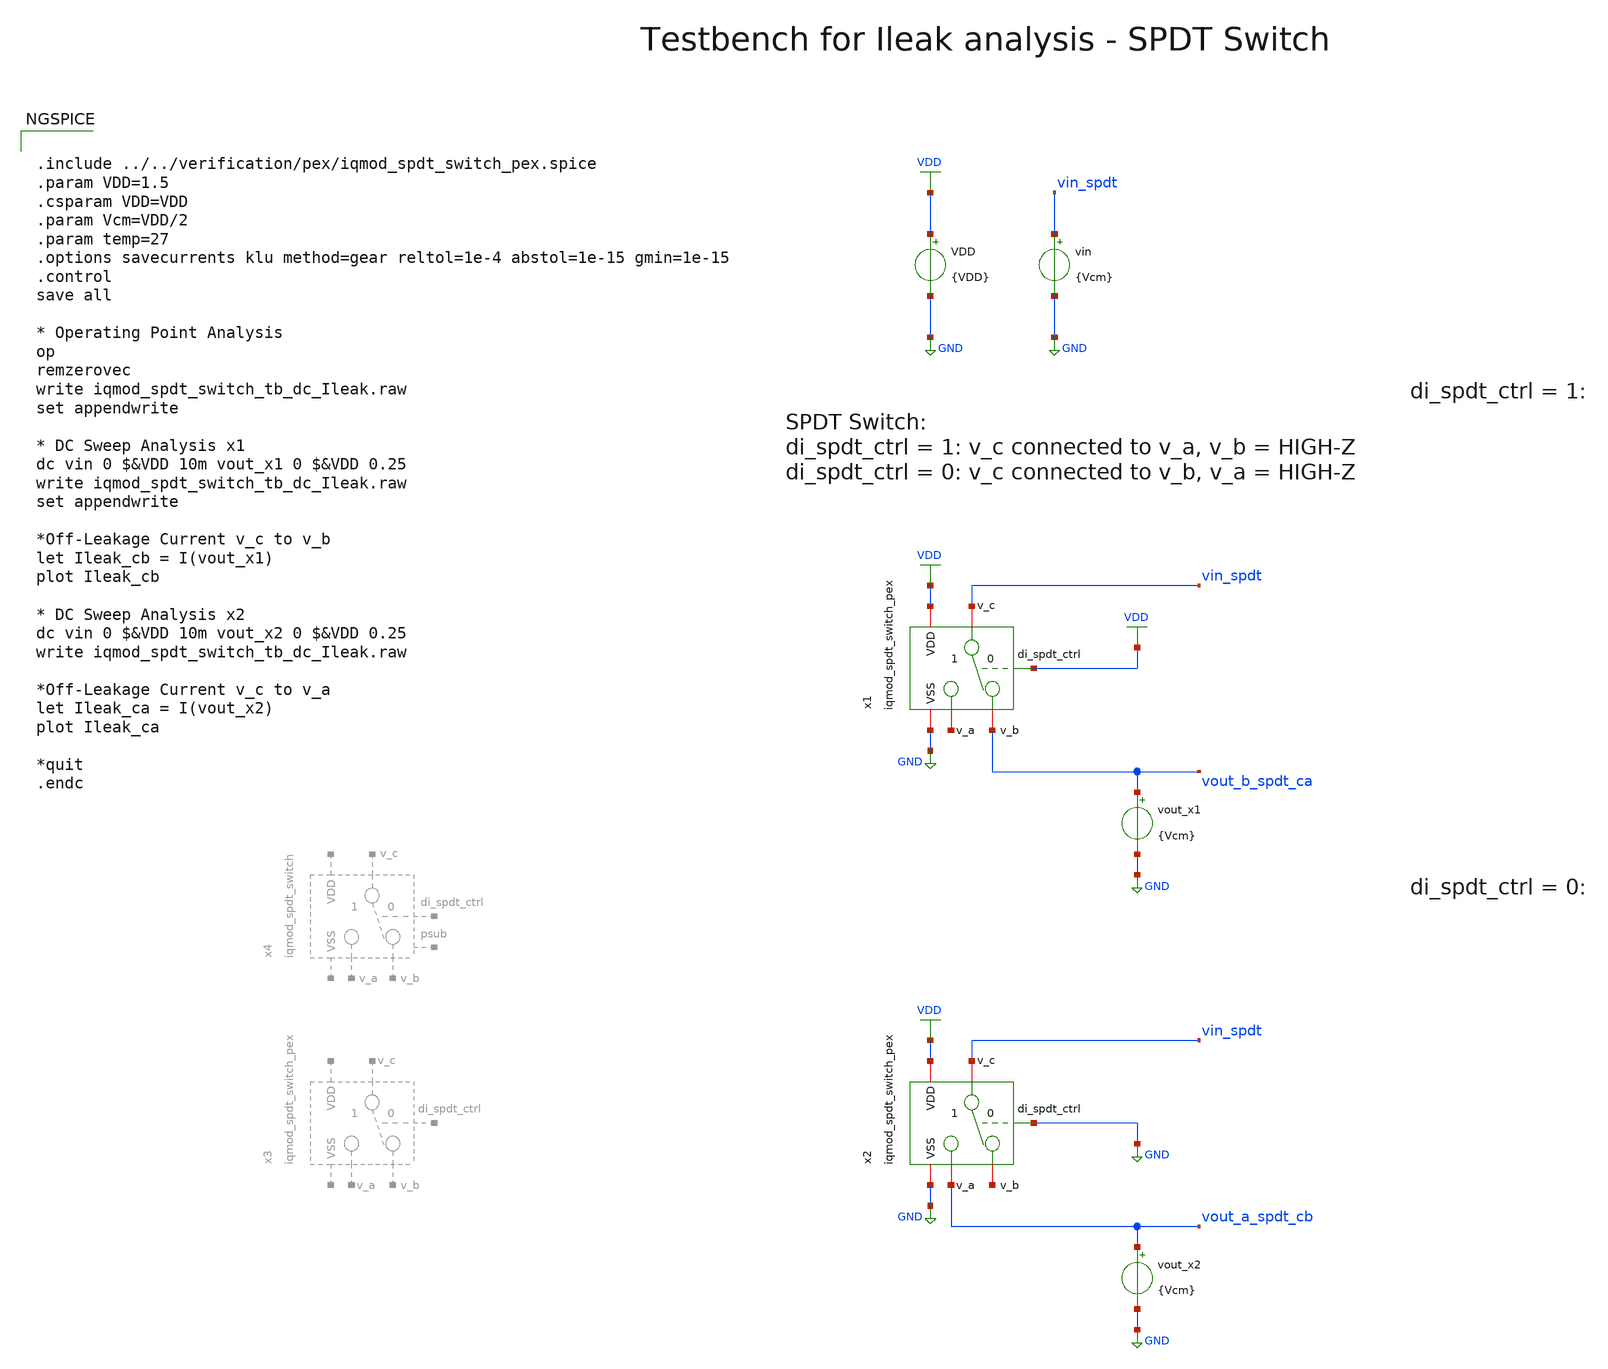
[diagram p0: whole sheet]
** sch_path: ihp130/macros/iqmod/xschem/testbenches/iqmod_spdt_switch_tb_dc_Ileak.sch
**.subckt iqmod_spdt_switch_tb_dc_Ileak
vout_x1 vout_b_spdt_ca GND {Vcm}
vout_x2 vout_a_spdt_cb GND {Vcm}
vin vin_spdt GND {Vcm}
VDD VDD GND {VDD}
x1 VDD VDD GND vin_spdt vout_b_spdt_ca net1 iqmod_spdt_switch_pex
x2 VDD GND GND vin_spdt net2 vout_a_spdt_cb iqmod_spdt_switch_pex
**** begin user architecture code


.include ../../verification/pex/iqmod_spdt_switch_pex.spice
.param VDD=1.5
.csparam VDD=VDD
.param Vcm=VDD/2
.param temp=27
.options savecurrents klu method=gear reltol=1e-4 abstol=1e-15 gmin=1e-15
.control
save all

* Operating Point Analysis
op
remzerovec
write iqmod_spdt_switch_tb_dc_Ileak.raw
set appendwrite

* DC Sweep Analysis x1
dc vin 0 $&VDD 10m vout_x1 0 $&VDD 0.25
write iqmod_spdt_switch_tb_dc_Ileak.raw
set appendwrite

*Off-Leakage Current v_c to v_b
let Ileak_cb = I(vout_x1)
plot Ileak_cb

* DC Sweep Analysis x2
dc vin 0 $&VDD 10m vout_x2 0 $&VDD 0.25
write iqmod_spdt_switch_tb_dc_Ileak.raw

*Off-Leakage Current v_c to v_a
let Ileak_ca = I(vout_x2)
plot Ileak_ca

*quit
.endc


.lib cornerMOSlv.lib mos_tt
.lib cornerMOShv.lib mos_tt
.lib cornerHBT.lib hbt_typ
.lib cornerRES.lib res_typ
.lib cornerCAP.lib cap_typ
.lib cornerDIO.lib dio_tt

**** end user architecture code
**.ends
.GLOBAL VDD
.GLOBAL GND
.end
